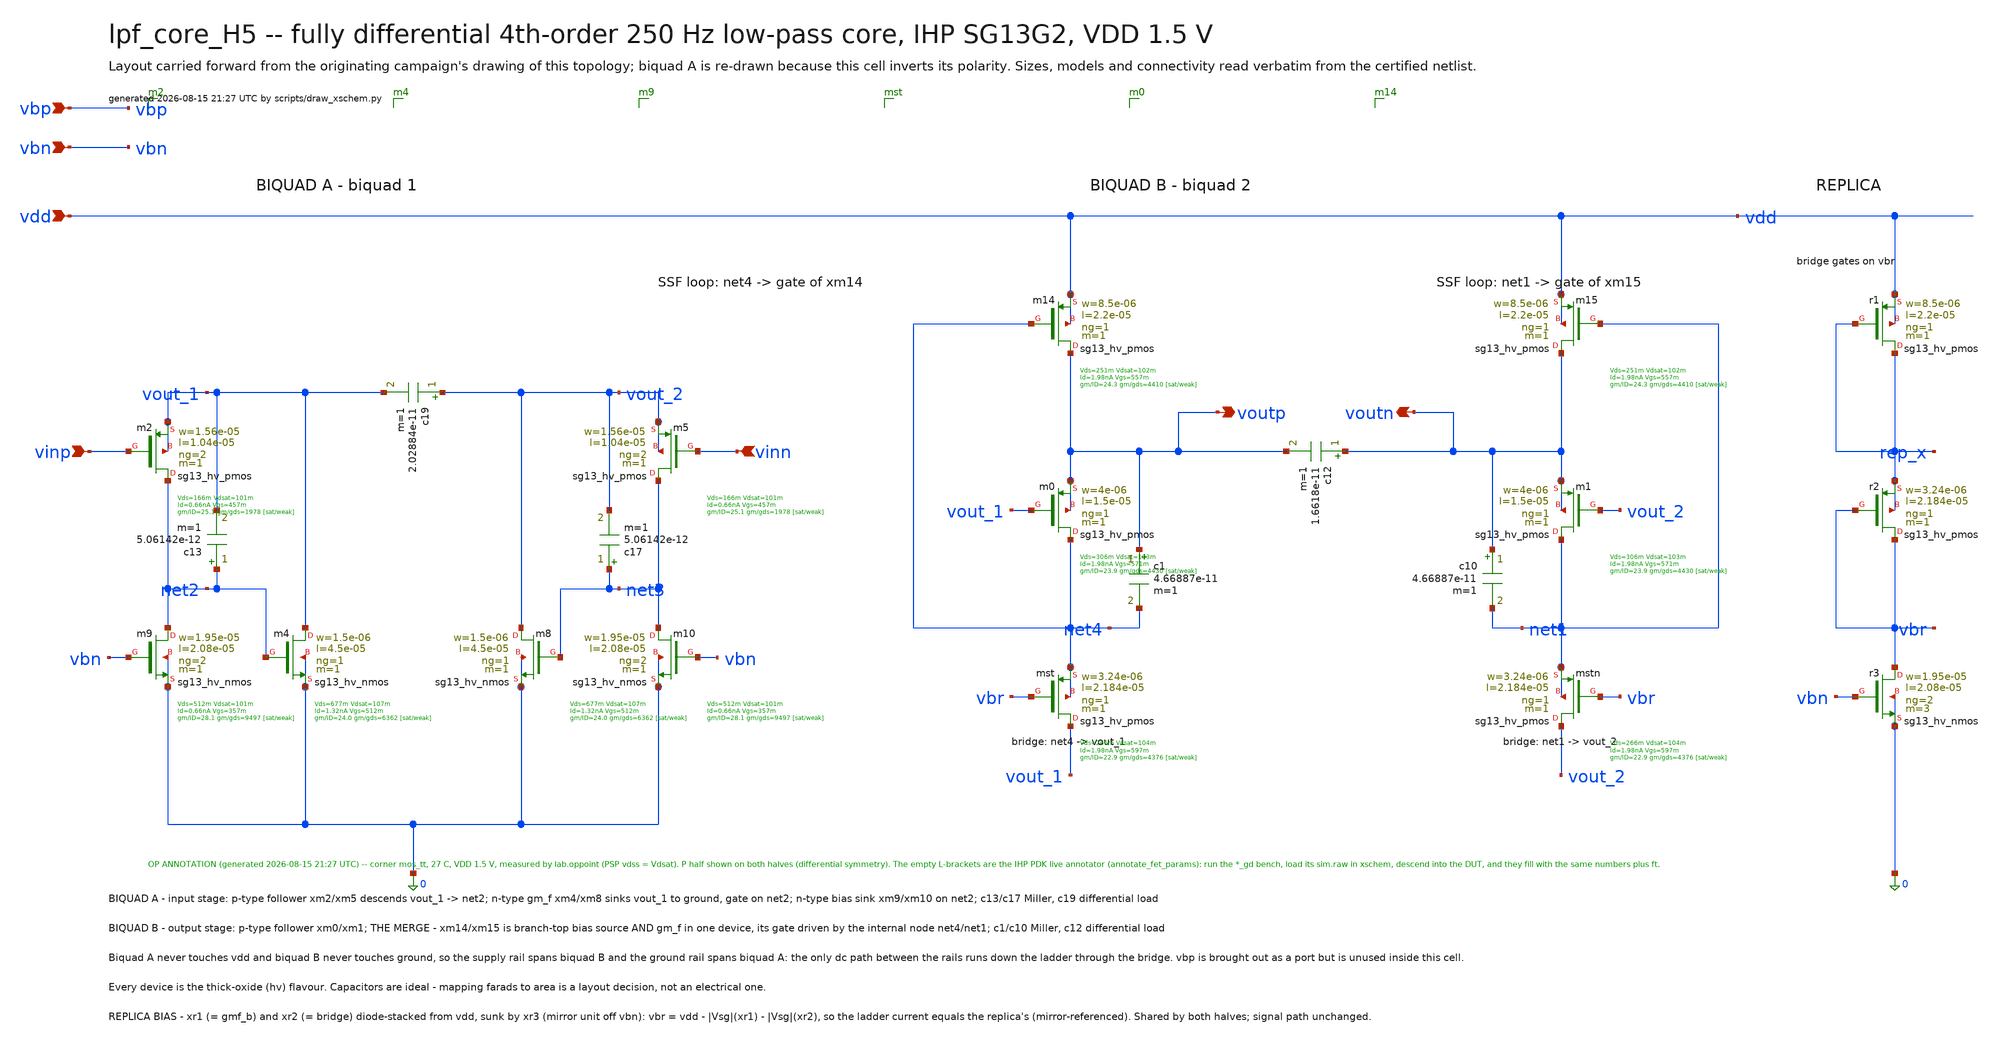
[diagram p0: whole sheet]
** sch_path: signoff/post-pvt/H5-lean/lpf_core_H5.sch
**.subckt lpf_core_H5 vinp vinn voutp voutn vdd vbn vbp
*.ipin vinp
*.ipin vinn
*.opin voutp
*.opin voutn
*.ipin vdd
*.ipin vbn
*.ipin vbp
Xm2 net2 vinp vout_1 vout_1 sg13_hv_pmos w=1.56e-05 l=1.04e-05 ng=2 m=1 mm_ok=1
Xm5 net3 vinn vout_2 vout_2 sg13_hv_pmos w=1.56e-05 l=1.04e-05 ng=2 m=1 mm_ok=1
Xm4 vout_1 net2 0 0 sg13_hv_nmos w=1.5e-06 l=4.5e-05 ng=1 m=1 mm_ok=1
Xm8 vout_2 net3 0 0 sg13_hv_nmos w=1.5e-06 l=4.5e-05 ng=1 m=1 mm_ok=1
Xm9 net2 vbn 0 0 sg13_hv_nmos w=1.95e-05 l=2.08e-05 ng=2 m=1 mm_ok=1
Xm10 net3 vbn 0 0 sg13_hv_nmos w=1.95e-05 l=2.08e-05 ng=2 m=1 mm_ok=1
Xmst vout_1 vbr net4 net4 sg13_hv_pmos w=3.24e-06 l=2.184e-05 ng=1 m=1 mm_ok=1
Xmstn vout_2 vbr net1 net1 sg13_hv_pmos w=3.24e-06 l=2.184e-05 ng=1 m=1 mm_ok=1
Xm0 net4 vout_1 voutp voutp sg13_hv_pmos w=4e-06 l=1.5e-05 ng=1 m=1 mm_ok=1
Xm1 net1 vout_2 voutn voutn sg13_hv_pmos w=4e-06 l=1.5e-05 ng=1 m=1 mm_ok=1
Xm14 voutp net4 vdd vdd sg13_hv_pmos w=8.5e-06 l=2.2e-05 ng=1 m=1 mm_ok=1
Xm15 voutn net1 vdd vdd sg13_hv_pmos w=8.5e-06 l=2.2e-05 ng=1 m=1 mm_ok=1
Xr1 rep_x rep_x vdd vdd sg13_hv_pmos w=8.5e-06 l=2.2e-05 ng=1 m=1 mm_ok=1
Xr2 vbr vbr rep_x rep_x sg13_hv_pmos w=3.24e-06 l=2.184e-05 ng=1 m=1 mm_ok=1
Xr3 vbr vbn 0 0 sg13_hv_nmos w=1.95e-05 l=2.08e-05 ng=2 m=3 mm_ok=1
c13 net2 vout_1 5.06142e-12 m=1
c17 net3 vout_2 5.06142e-12 m=1
c19 vout_2 vout_1 2.02884e-11 m=1
c1 voutp net4 4.66887e-11 m=1
c10 voutn net1 4.66887e-11 m=1
c12 voutn voutp 1.6618e-11 m=1
**.ends
.end
